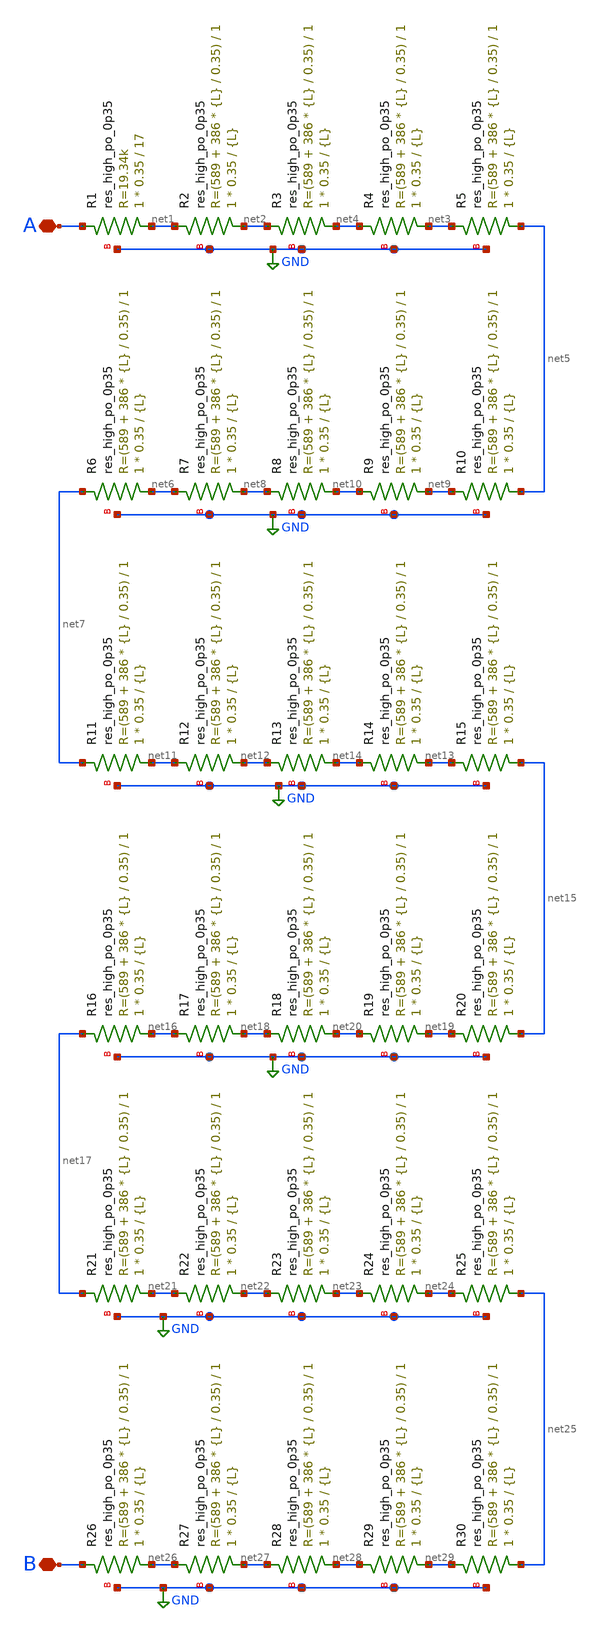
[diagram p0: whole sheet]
** sch_path: xschem/ResistorStart.sch
**.subckt ResistorStart A B
*.iopin A
*.iopin B
XR1 net1 A GND sky130_fd_pr__res_high_po_0p35 L=17 mult=1 m=1
XR2 net2 net1 GND sky130_fd_pr__res_high_po_0p35 L={L} mult=1 m=1
XR3 net4 net2 GND sky130_fd_pr__res_high_po_0p35 L={L} mult=1 m=1
XR4 net3 net4 GND sky130_fd_pr__res_high_po_0p35 L={L} mult=1 m=1
XR5 net5 net3 GND sky130_fd_pr__res_high_po_0p35 L={L} mult=1 m=1
XR6 net6 net7 GND sky130_fd_pr__res_high_po_0p35 L={L} mult=1 m=1
XR7 net8 net6 GND sky130_fd_pr__res_high_po_0p35 L={L} mult=1 m=1
XR8 net10 net8 GND sky130_fd_pr__res_high_po_0p35 L={L} mult=1 m=1
XR9 net9 net10 GND sky130_fd_pr__res_high_po_0p35 L={L} mult=1 m=1
XR10 net5 net9 GND sky130_fd_pr__res_high_po_0p35 L={L} mult=1 m=1
XR11 net11 net7 GND sky130_fd_pr__res_high_po_0p35 L={L} mult=1 m=1
XR12 net12 net11 GND sky130_fd_pr__res_high_po_0p35 L={L} mult=1 m=1
XR13 net14 net12 GND sky130_fd_pr__res_high_po_0p35 L={L} mult=1 m=1
XR14 net13 net14 GND sky130_fd_pr__res_high_po_0p35 L={L} mult=1 m=1
XR15 net15 net13 GND sky130_fd_pr__res_high_po_0p35 L={L} mult=1 m=1
XR16 net16 net17 GND sky130_fd_pr__res_high_po_0p35 L={L} mult=1 m=1
XR17 net18 net16 GND sky130_fd_pr__res_high_po_0p35 L={L} mult=1 m=1
XR18 net20 net18 GND sky130_fd_pr__res_high_po_0p35 L={L} mult=1 m=1
XR19 net19 net20 GND sky130_fd_pr__res_high_po_0p35 L={L} mult=1 m=1
XR20 net15 net19 GND sky130_fd_pr__res_high_po_0p35 L={L} mult=1 m=1
XR21 net21 net17 GND sky130_fd_pr__res_high_po_0p35 L={L} mult=1 m=1
XR22 net22 net21 GND sky130_fd_pr__res_high_po_0p35 L={L} mult=1 m=1
XR23 net23 net22 GND sky130_fd_pr__res_high_po_0p35 L={L} mult=1 m=1
XR24 net24 net23 GND sky130_fd_pr__res_high_po_0p35 L={L} mult=1 m=1
XR25 net25 net24 GND sky130_fd_pr__res_high_po_0p35 L={L} mult=1 m=1
XR26 net26 B GND sky130_fd_pr__res_high_po_0p35 L={L} mult=1 m=1
XR27 net27 net26 GND sky130_fd_pr__res_high_po_0p35 L={L} mult=1 m=1
XR28 net28 net27 GND sky130_fd_pr__res_high_po_0p35 L={L} mult=1 m=1
XR29 net29 net28 GND sky130_fd_pr__res_high_po_0p35 L={L} mult=1 m=1
XR30 net25 net29 GND sky130_fd_pr__res_high_po_0p35 L={L} mult=1 m=1
**** begin user architecture code


.param L=17


**** end user architecture code
**.ends
.GLOBAL GND
.end
